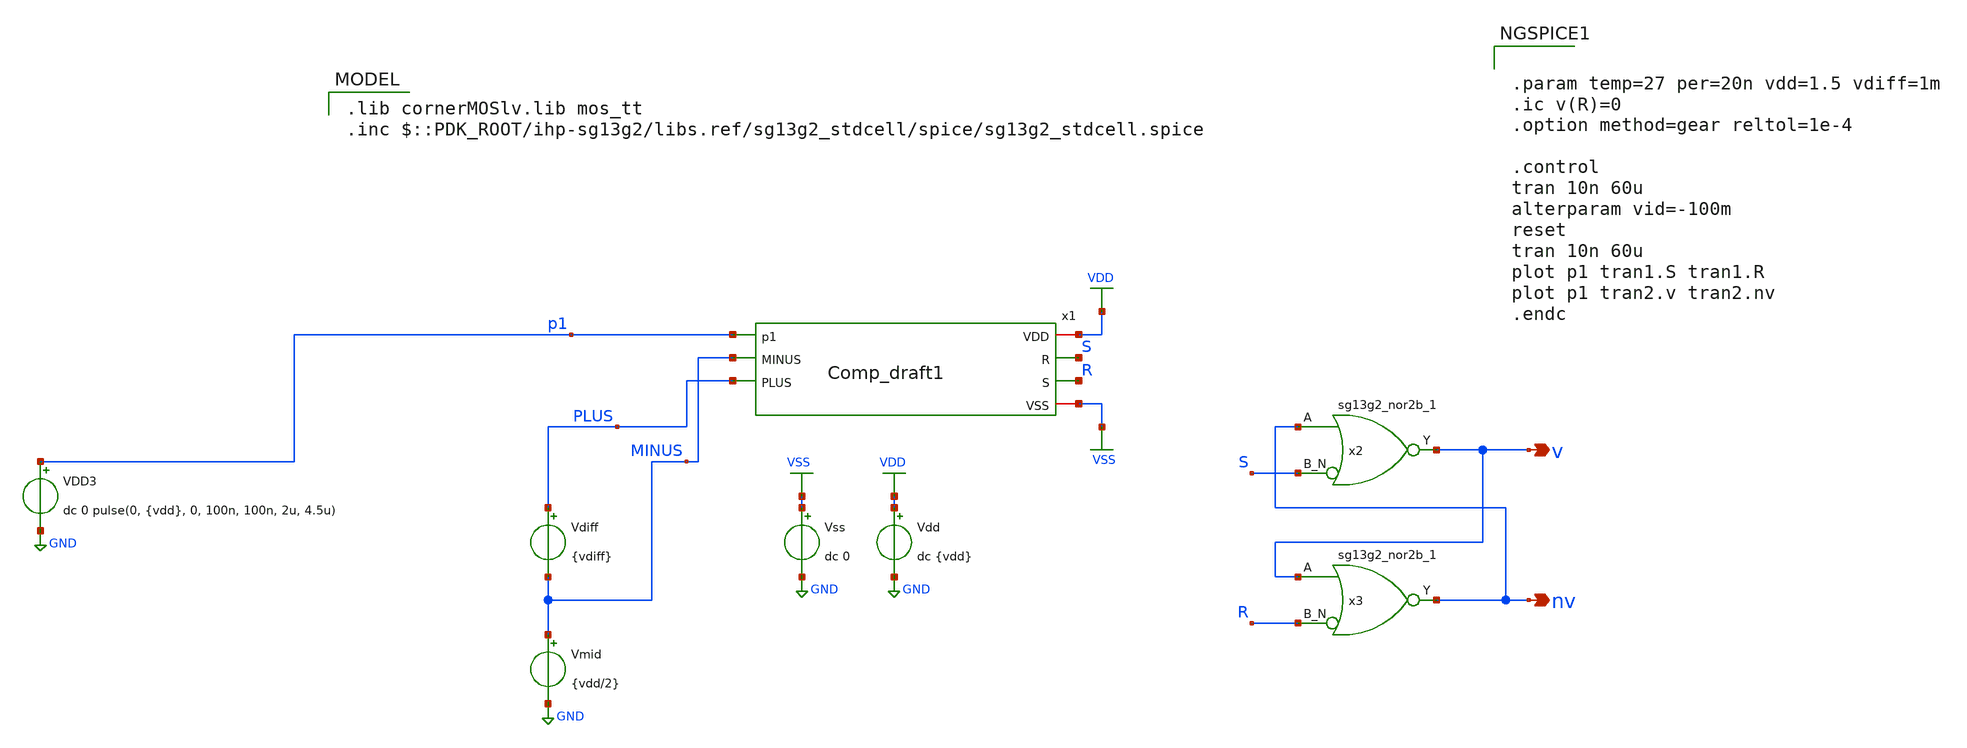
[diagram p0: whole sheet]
** sch_path: DSM/Schematics/Comparator_design_Sneha/COMPARATOR_FINAL/tb_Comp_Latch.sch
**.subckt tb_Comp_Latch v nv
*.opin v
*.opin nv
Vdd VDD GND dc {vdd}
Vss VSS GND dc 0
VDD3 p1 GND dc 0 pulse(0, {vdd}, 0, 100n, 100n, 2u, 4.5u)
Vdiff PLUS MINUS {vdiff}
Vmid MINUS GND {vdd/2}
x2 v nv S VDD VSS sg13g2_nor2b_1
x3 nv v R VDD VSS sg13g2_nor2b_1
x1 VDD p1 S R MINUS PLUS VSS Comp_draft1
**** begin user architecture code
 .lib cornerMOSlv.lib mos_tt
.inc $::PDK_ROOT/ihp-sg13g2/libs.ref/sg13g2_stdcell/spice/sg13g2_stdcell.spice


.param temp=27 per=20n vdd=1.5 vdiff=1m
.ic v(R)=0
.option method=gear reltol=1e-4

.control
tran 10n 60u
alterparam vid=-100m
reset
tran 10n 60u
plot p1 tran1.S tran1.R
plot p1 tran2.v tran2.nv
.endc


**** end user architecture code
**.ends

* expanding   symbol:  sg13g2_stdcells/sg13g2_nor2b_1.sym # of pins=3
** sym_path: sg13g2_stdcells/sg13g2_nor2b_1.sym
** sch_path: sg13g2_stdcells/sg13g2_nor2b_1.sch
.subckt sg13g2_nor2b_1 Y A B_N VDD VSS
*.opin Y
*.ipin B_N
*.ipin A
*.iopin VDD
*.iopin VSS
XM1 B B_N VSS VSS sg13_lv_nmos w=550.00n l=130.00n ng=1 m=1 mm_ok=1
XM2 Y A VSS VSS sg13_lv_nmos w=740.00n l=130.00n ng=1 m=1 mm_ok=1
XM3 Y B VSS VSS sg13_lv_nmos w=740.00n l=130.00n ng=1 m=1 mm_ok=1
XM4 B B_N VDD VDD sg13_lv_pmos w=840.00n l=130.00n ng=1 m=1 mm_ok=1
XM5 net1 B VDD VDD sg13_lv_pmos w=1.12u l=130.00n ng=1 m=1 mm_ok=1
XM6 Y A net1 VDD sg13_lv_pmos w=1.12u l=130.00n ng=1 m=1 mm_ok=1
.ends


* expanding   symbol:  Comp_draft1.sym # of pins=7
** sym_path: DSM/Schematics/Comparator_design_Sneha/COMPARATOR_FINAL/Comp_draft1.sym
** sch_path: DSM/Schematics/Comparator_design_Sneha/COMPARATOR_FINAL/Comp_draft1.sch
.subckt Comp_draft1 VDD p1 R S MINUS PLUS VSS
*.ipin PLUS
*.ipin MINUS
*.ipin p1
*.iopin VDD
*.iopin VSS
*.opin R
*.opin S
XMN5 S R net3 VSS sg13_lv_nmos w=1u l=0.18u ng=1 m=1 mm_ok=1
XMP7 net3 p1 VDD VDD sg13_lv_pmos w=0.5u l=0.18u ng=1 m=1 mm_ok=1
XMP8 S p1 VDD VDD sg13_lv_pmos w=0.5u l=0.18u ng=1 m=1 mm_ok=1
XMP9 S R VDD VDD sg13_lv_pmos w=2u l=0.18u ng=1 m=1 mm_ok=1
XMP10 R S VDD VDD sg13_lv_pmos w=2u l=0.18u ng=1 m=1 mm_ok=1
XMP11 R p1 VDD VDD sg13_lv_pmos w=0.5u l=0.18u ng=1 m=1 mm_ok=1
XMP12 net2 p1 VDD VDD sg13_lv_pmos w=0.5u l=0.15u ng=1 m=1 mm_ok=1
XMN6 R S net2 VSS sg13_lv_nmos w=1u l=0.18u ng=1 m=1 mm_ok=1
XMN7 net4 PLUS net1 VSS sg13_lv_nmos w=2u l=0.18u ng=1 m=1 mm_ok=1
XMN8 net2 MINUS net1 VSS sg13_lv_nmos w=2u l=0.18u ng=1 m=1 mm_ok=1
XM7 net1 p1 VSS VSS sg13_lv_nmos w=4u l=0.18u ng=1 m=1 mm_ok=1
.ends

.GLOBAL GND
.GLOBAL VDD
.GLOBAL VSS
.end
